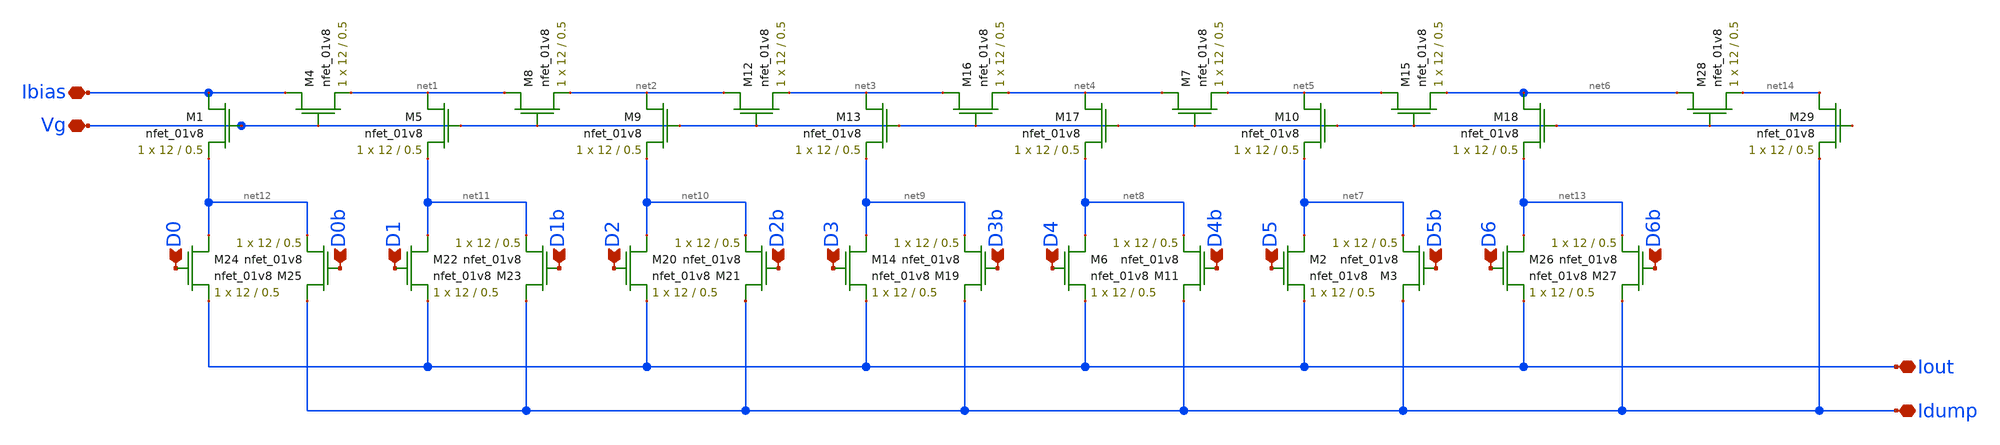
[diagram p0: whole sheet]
** sch_path: schematics/ieee DAC/ieee_DAC.sch
**.subckt ieee_DAC D0 D1 D2 D3 D4 D5 D6 D0b D1b D2b D3b D4b D5b D6b Iout Idump Ibias Vg
*.ipin D0
*.ipin D1
*.ipin D2
*.ipin D3
*.ipin D4
*.ipin D5
*.ipin D6
*.ipin D0b
*.ipin D1b
*.ipin D2b
*.ipin D3b
*.ipin D4b
*.ipin D5b
*.ipin D6b
*.iopin Iout
*.iopin Idump
*.iopin Ibias
*.iopin Vg
XM1 Ibias Vg net12 GND sky130_fd_pr__nfet_01v8 L=0.5 W=12 nf=1 ad='int((nf+1)/2) * W/nf * 0.29' as='int((nf+2)/2) * W/nf * 0.29'
+ pd='2*int((nf+1)/2) * (W/nf + 0.29)' ps='2*int((nf+2)/2) * (W/nf + 0.29)' nrd='0.29 / W' nrs='0.29 / W'
+ sa=0 sb=0 sd=0 mult=1 m=1
XM4 Ibias Vg net1 GND sky130_fd_pr__nfet_01v8 L=0.5 W=12 nf=1 ad='int((nf+1)/2) * W/nf * 0.29' as='int((nf+2)/2) * W/nf * 0.29'
+ pd='2*int((nf+1)/2) * (W/nf + 0.29)' ps='2*int((nf+2)/2) * (W/nf + 0.29)' nrd='0.29 / W' nrs='0.29 / W'
+ sa=0 sb=0 sd=0 mult=1 m=1
XM5 net1 Vg net11 GND sky130_fd_pr__nfet_01v8 L=0.5 W=12 nf=1 ad='int((nf+1)/2) * W/nf * 0.29' as='int((nf+2)/2) * W/nf * 0.29'
+ pd='2*int((nf+1)/2) * (W/nf + 0.29)' ps='2*int((nf+2)/2) * (W/nf + 0.29)' nrd='0.29 / W' nrs='0.29 / W'
+ sa=0 sb=0 sd=0 mult=1 m=1
XM8 net1 Vg net2 GND sky130_fd_pr__nfet_01v8 L=0.5 W=12 nf=1 ad='int((nf+1)/2) * W/nf * 0.29' as='int((nf+2)/2) * W/nf * 0.29'
+ pd='2*int((nf+1)/2) * (W/nf + 0.29)' ps='2*int((nf+2)/2) * (W/nf + 0.29)' nrd='0.29 / W' nrs='0.29 / W'
+ sa=0 sb=0 sd=0 mult=1 m=1
XM9 net2 Vg net10 GND sky130_fd_pr__nfet_01v8 L=0.5 W=12 nf=1 ad='int((nf+1)/2) * W/nf * 0.29' as='int((nf+2)/2) * W/nf * 0.29'
+ pd='2*int((nf+1)/2) * (W/nf + 0.29)' ps='2*int((nf+2)/2) * (W/nf + 0.29)' nrd='0.29 / W' nrs='0.29 / W'
+ sa=0 sb=0 sd=0 mult=1 m=1
XM12 net2 Vg net3 GND sky130_fd_pr__nfet_01v8 L=0.5 W=12 nf=1 ad='int((nf+1)/2) * W/nf * 0.29' as='int((nf+2)/2) * W/nf * 0.29'
+ pd='2*int((nf+1)/2) * (W/nf + 0.29)' ps='2*int((nf+2)/2) * (W/nf + 0.29)' nrd='0.29 / W' nrs='0.29 / W'
+ sa=0 sb=0 sd=0 mult=1 m=1
XM13 net3 Vg net9 GND sky130_fd_pr__nfet_01v8 L=0.5 W=12 nf=1 ad='int((nf+1)/2) * W/nf * 0.29' as='int((nf+2)/2) * W/nf * 0.29'
+ pd='2*int((nf+1)/2) * (W/nf + 0.29)' ps='2*int((nf+2)/2) * (W/nf + 0.29)' nrd='0.29 / W' nrs='0.29 / W'
+ sa=0 sb=0 sd=0 mult=1 m=1
XM16 net3 Vg net4 GND sky130_fd_pr__nfet_01v8 L=0.5 W=12 nf=1 ad='int((nf+1)/2) * W/nf * 0.29' as='int((nf+2)/2) * W/nf * 0.29'
+ pd='2*int((nf+1)/2) * (W/nf + 0.29)' ps='2*int((nf+2)/2) * (W/nf + 0.29)' nrd='0.29 / W' nrs='0.29 / W'
+ sa=0 sb=0 sd=0 mult=1 m=1
XM17 net4 Vg net8 GND sky130_fd_pr__nfet_01v8 L=0.5 W=12 nf=1 ad='int((nf+1)/2) * W/nf * 0.29' as='int((nf+2)/2) * W/nf * 0.29'
+ pd='2*int((nf+1)/2) * (W/nf + 0.29)' ps='2*int((nf+2)/2) * (W/nf + 0.29)' nrd='0.29 / W' nrs='0.29 / W'
+ sa=0 sb=0 sd=0 mult=1 m=1
XM7 net4 Vg net5 GND sky130_fd_pr__nfet_01v8 L=0.5 W=12 nf=1 ad='int((nf+1)/2) * W/nf * 0.29' as='int((nf+2)/2) * W/nf * 0.29'
+ pd='2*int((nf+1)/2) * (W/nf + 0.29)' ps='2*int((nf+2)/2) * (W/nf + 0.29)' nrd='0.29 / W' nrs='0.29 / W'
+ sa=0 sb=0 sd=0 mult=1 m=1
XM10 net5 Vg net7 GND sky130_fd_pr__nfet_01v8 L=0.5 W=12 nf=1 ad='int((nf+1)/2) * W/nf * 0.29' as='int((nf+2)/2) * W/nf * 0.29'
+ pd='2*int((nf+1)/2) * (W/nf + 0.29)' ps='2*int((nf+2)/2) * (W/nf + 0.29)' nrd='0.29 / W' nrs='0.29 / W'
+ sa=0 sb=0 sd=0 mult=1 m=1
XM15 net5 Vg net6 GND sky130_fd_pr__nfet_01v8 L=0.5 W=12 nf=1 ad='int((nf+1)/2) * W/nf * 0.29' as='int((nf+2)/2) * W/nf * 0.29'
+ pd='2*int((nf+1)/2) * (W/nf + 0.29)' ps='2*int((nf+2)/2) * (W/nf + 0.29)' nrd='0.29 / W' nrs='0.29 / W'
+ sa=0 sb=0 sd=0 mult=1 m=1
XM18 net6 Vg net13 GND sky130_fd_pr__nfet_01v8 L=0.5 W=12 nf=1 ad='int((nf+1)/2) * W/nf * 0.29' as='int((nf+2)/2) * W/nf * 0.29'
+ pd='2*int((nf+1)/2) * (W/nf + 0.29)' ps='2*int((nf+2)/2) * (W/nf + 0.29)' nrd='0.29 / W' nrs='0.29 / W'
+ sa=0 sb=0 sd=0 mult=1 m=1
XM2 net7 D5 Iout GND sky130_fd_pr__nfet_01v8 L=0.5 W=12 nf=1 ad='int((nf+1)/2) * W/nf * 0.29' as='int((nf+2)/2) * W/nf * 0.29'
+ pd='2*int((nf+1)/2) * (W/nf + 0.29)' ps='2*int((nf+2)/2) * (W/nf + 0.29)' nrd='0.29 / W' nrs='0.29 / W'
+ sa=0 sb=0 sd=0 mult=1 m=1
XM3 Idump D5b net7 GND sky130_fd_pr__nfet_01v8 L=0.5 W=12 nf=1 ad='int((nf+1)/2) * W/nf * 0.29' as='int((nf+2)/2) * W/nf * 0.29'
+ pd='2*int((nf+1)/2) * (W/nf + 0.29)' ps='2*int((nf+2)/2) * (W/nf + 0.29)' nrd='0.29 / W' nrs='0.29 / W'
+ sa=0 sb=0 sd=0 mult=1 m=1
XM6 net8 D4 Iout GND sky130_fd_pr__nfet_01v8 L=0.5 W=12 nf=1 ad='int((nf+1)/2) * W/nf * 0.29' as='int((nf+2)/2) * W/nf * 0.29'
+ pd='2*int((nf+1)/2) * (W/nf + 0.29)' ps='2*int((nf+2)/2) * (W/nf + 0.29)' nrd='0.29 / W' nrs='0.29 / W'
+ sa=0 sb=0 sd=0 mult=1 m=1
XM11 Idump D4b net8 GND sky130_fd_pr__nfet_01v8 L=0.5 W=12 nf=1 ad='int((nf+1)/2) * W/nf * 0.29' as='int((nf+2)/2) * W/nf * 0.29'
+ pd='2*int((nf+1)/2) * (W/nf + 0.29)' ps='2*int((nf+2)/2) * (W/nf + 0.29)' nrd='0.29 / W' nrs='0.29 / W'
+ sa=0 sb=0 sd=0 mult=1 m=1
XM14 net9 D3 Iout GND sky130_fd_pr__nfet_01v8 L=0.5 W=12 nf=1 ad='int((nf+1)/2) * W/nf * 0.29' as='int((nf+2)/2) * W/nf * 0.29'
+ pd='2*int((nf+1)/2) * (W/nf + 0.29)' ps='2*int((nf+2)/2) * (W/nf + 0.29)' nrd='0.29 / W' nrs='0.29 / W'
+ sa=0 sb=0 sd=0 mult=1 m=1
XM19 Idump D3b net9 GND sky130_fd_pr__nfet_01v8 L=0.5 W=12 nf=1 ad='int((nf+1)/2) * W/nf * 0.29' as='int((nf+2)/2) * W/nf * 0.29'
+ pd='2*int((nf+1)/2) * (W/nf + 0.29)' ps='2*int((nf+2)/2) * (W/nf + 0.29)' nrd='0.29 / W' nrs='0.29 / W'
+ sa=0 sb=0 sd=0 mult=1 m=1
XM20 net10 D2 Iout GND sky130_fd_pr__nfet_01v8 L=0.5 W=12 nf=1 ad='int((nf+1)/2) * W/nf * 0.29' as='int((nf+2)/2) * W/nf * 0.29'
+ pd='2*int((nf+1)/2) * (W/nf + 0.29)' ps='2*int((nf+2)/2) * (W/nf + 0.29)' nrd='0.29 / W' nrs='0.29 / W'
+ sa=0 sb=0 sd=0 mult=1 m=1
XM21 Idump D2b net10 GND sky130_fd_pr__nfet_01v8 L=0.5 W=12 nf=1 ad='int((nf+1)/2) * W/nf * 0.29' as='int((nf+2)/2) * W/nf * 0.29'
+ pd='2*int((nf+1)/2) * (W/nf + 0.29)' ps='2*int((nf+2)/2) * (W/nf + 0.29)' nrd='0.29 / W' nrs='0.29 / W'
+ sa=0 sb=0 sd=0 mult=1 m=1
XM22 net11 D1 Iout GND sky130_fd_pr__nfet_01v8 L=0.5 W=12 nf=1 ad='int((nf+1)/2) * W/nf * 0.29' as='int((nf+2)/2) * W/nf * 0.29'
+ pd='2*int((nf+1)/2) * (W/nf + 0.29)' ps='2*int((nf+2)/2) * (W/nf + 0.29)' nrd='0.29 / W' nrs='0.29 / W'
+ sa=0 sb=0 sd=0 mult=1 m=1
XM23 Idump D1b net11 GND sky130_fd_pr__nfet_01v8 L=0.5 W=12 nf=1 ad='int((nf+1)/2) * W/nf * 0.29' as='int((nf+2)/2) * W/nf * 0.29'
+ pd='2*int((nf+1)/2) * (W/nf + 0.29)' ps='2*int((nf+2)/2) * (W/nf + 0.29)' nrd='0.29 / W' nrs='0.29 / W'
+ sa=0 sb=0 sd=0 mult=1 m=1
XM24 net12 D0 Iout GND sky130_fd_pr__nfet_01v8 L=0.5 W=12 nf=1 ad='int((nf+1)/2) * W/nf * 0.29' as='int((nf+2)/2) * W/nf * 0.29'
+ pd='2*int((nf+1)/2) * (W/nf + 0.29)' ps='2*int((nf+2)/2) * (W/nf + 0.29)' nrd='0.29 / W' nrs='0.29 / W'
+ sa=0 sb=0 sd=0 mult=1 m=1
XM25 Idump D0b net12 GND sky130_fd_pr__nfet_01v8 L=0.5 W=12 nf=1 ad='int((nf+1)/2) * W/nf * 0.29' as='int((nf+2)/2) * W/nf * 0.29'
+ pd='2*int((nf+1)/2) * (W/nf + 0.29)' ps='2*int((nf+2)/2) * (W/nf + 0.29)' nrd='0.29 / W' nrs='0.29 / W'
+ sa=0 sb=0 sd=0 mult=1 m=1
XM26 net13 D6 Iout GND sky130_fd_pr__nfet_01v8 L=0.5 W=12 nf=1 ad='int((nf+1)/2) * W/nf * 0.29' as='int((nf+2)/2) * W/nf * 0.29'
+ pd='2*int((nf+1)/2) * (W/nf + 0.29)' ps='2*int((nf+2)/2) * (W/nf + 0.29)' nrd='0.29 / W' nrs='0.29 / W'
+ sa=0 sb=0 sd=0 mult=1 m=1
XM27 Idump D6b net13 GND sky130_fd_pr__nfet_01v8 L=0.5 W=12 nf=1 ad='int((nf+1)/2) * W/nf * 0.29' as='int((nf+2)/2) * W/nf * 0.29'
+ pd='2*int((nf+1)/2) * (W/nf + 0.29)' ps='2*int((nf+2)/2) * (W/nf + 0.29)' nrd='0.29 / W' nrs='0.29 / W'
+ sa=0 sb=0 sd=0 mult=1 m=1
XM28 net6 Vg net14 GND sky130_fd_pr__nfet_01v8 L=0.5 W=12 nf=1 ad='int((nf+1)/2) * W/nf * 0.29' as='int((nf+2)/2) * W/nf * 0.29'
+ pd='2*int((nf+1)/2) * (W/nf + 0.29)' ps='2*int((nf+2)/2) * (W/nf + 0.29)' nrd='0.29 / W' nrs='0.29 / W'
+ sa=0 sb=0 sd=0 mult=1 m=1
XM29 net14 Vg Idump GND sky130_fd_pr__nfet_01v8 L=0.5 W=12 nf=1 ad='int((nf+1)/2) * W/nf * 0.29' as='int((nf+2)/2) * W/nf * 0.29'
+ pd='2*int((nf+1)/2) * (W/nf + 0.29)' ps='2*int((nf+2)/2) * (W/nf + 0.29)' nrd='0.29 / W' nrs='0.29 / W'
+ sa=0 sb=0 sd=0 mult=1 m=1
**.ends
.end
